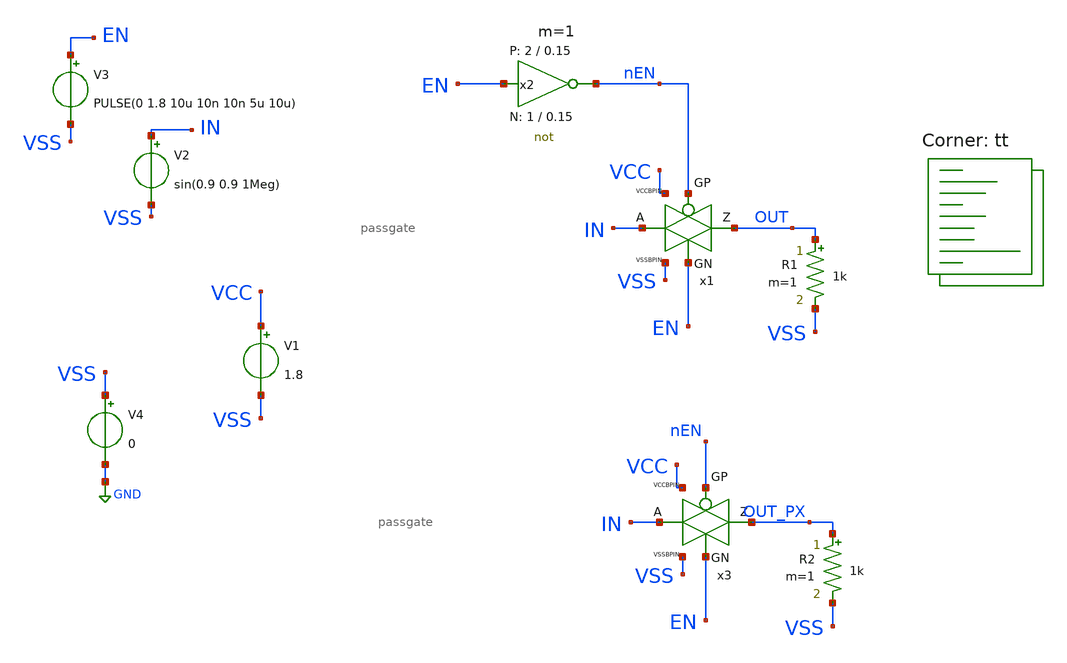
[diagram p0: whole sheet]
** sch_path: xschem/tb_passgate.sch
* StefanSchippers/xschem_sky130/sky130_tests/not.sch:
* Copyright 2021 Stefan Frederik Schippers
* Licensed under the Apache License, Version 2.0 (the "License");
**.subckt tb_passgate
x1 OUT IN nEN EN VSS VCC passgate
V1 VCC VSS 1.8
x2 nEN EN VCC VSS not W_N=1 L_N=0.15 W_P=2 L_P=0.15 m=1
V2 IN VSS sin(0.9 0.9 1Meg)
V3 EN VSS PULSE(0 1.8 10u 10n 10n 5u 10u)
R1 OUT VSS 1k m=1
V4 VSS GND 0
x3 OUT_PX IN nEN EN VSS VCC passgate_parax
R2 OUT_PX VSS 1k m=1
**** begin user architecture code
.lib $::SKYWATER_MODELS/sky130.lib.spice tt
**** end user architecture code
**.ends

* expanding   symbol:  /home/ttuser/tt08-wowa2/xschem/passgate.sym # of pins=6
** sym_path: xschem/passgate.sym
** sch_path: xschem/passgate.sch
.subckt passgate Z A GP GN VSSBPIN VCCBPIN
*.ipin GN
*.ipin VCCBPIN
*.ipin VSSBPIN
*.ipin GP
*.iopin A
*.iopin Z
XM1 Z GN A VSSBPIN sky130_fd_pr__nfet_01v8_lvt L=0.35 W=8 nf=1 ad='int((nf+1)/2) * W/nf * 0.29' as='int((nf+2)/2) * W/nf * 0.29'
+ pd='2*int((nf+1)/2) * (W/nf + 0.29)' ps='2*int((nf+2)/2) * (W/nf + 0.29)' nrd='0.29 / W' nrs='0.29 / W'
+ sa=0 sb=0 sd=0 mult=2 m=2
XM3 Z GP A VCCBPIN sky130_fd_pr__pfet_01v8_lvt L=0.35 W=10 nf=1 ad='int((nf+1)/2) * W/nf * 0.29' as='int((nf+2)/2) * W/nf * 0.29'
+ pd='2*int((nf+1)/2) * (W/nf + 0.29)' ps='2*int((nf+2)/2) * (W/nf + 0.29)' nrd='0.29 / W' nrs='0.29 / W'
+ sa=0 sb=0 sd=0 mult=2 m=2
.ends


* expanding   symbol:  sky130_tests/not.sym # of pins=2
** sym_path: sky130_tests/not.sym
** sch_path: sky130_tests/not.sch
.subckt not y a VCCPIN VSSPIN     W_N=1 L_N=0.15 W_P=2 L_P=0.15
*.opin y
*.ipin a
XM1 DN a VSSPIN VSSPIN sky130_fd_pr__nfet_01v8 L=L_N W=W_N nf=1 ad='int((1 + 1)/2) * W_N / 1 * 0.29'
+ as='int((1 + 2)/2) * W_N / 1 * 0.29' pd='2*int((1 + 1)/2) * (W_N / 1 + 0.29)' ps='2*int((1 + 2)/2) * (W_N / 1 + 0.29)'
+ nrd='0.29 / W_N ' nrs='0.29 / W_N ' sa=0 sb=0 sd=0 mult=1 m=1
XM2 DP a VCCPIN VCCPIN sky130_fd_pr__pfet_01v8 L=L_P W=W_P nf=1 ad='int((nf+1)/2) * W/nf * 0.29' as='int((nf+2)/2) * W/nf * 0.29'
+ pd='2*int((nf+1)/2) * (W/nf + 0.29)' ps='2*int((nf+2)/2) * (W/nf + 0.29)' nrd='0.29 / W' nrs='0.29 / W'
+ sa=0 sb=0 sd=0 mult=1 m=1
Vmeas DP y 0
.save i(vmeas)
Vmeas1 y DN 0
.save i(vmeas1)
.save v(dp)
.save v(dn)
.ends


* expanding   symbol:  /home/ttuser/tt08-wowa2/xschem/passgate_parax.sym # of pins=6
** sym_path: xschem/passgate.sym
.include [file normalize extracted/passgate_parax.spice]
.GLOBAL GND
**** begin user architecture code


* ngspice commands
* .options savecurrents

.control
save all
op
write tb_passgate.raw
set appendwrite
tran 10n 50u
write tb_passgate.raw
quit 0
.endc



**** end user architecture code
.end
